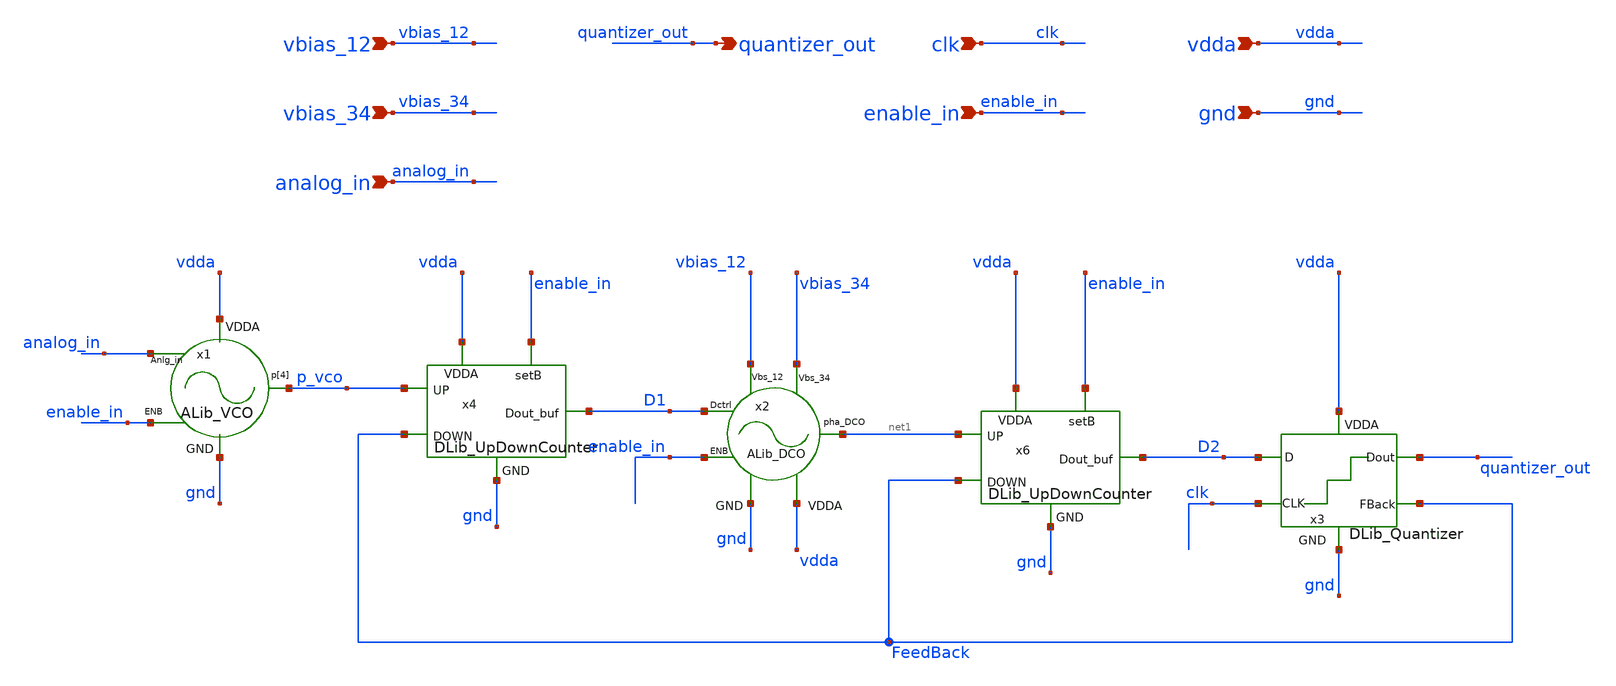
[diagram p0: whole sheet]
** sch_path: xschem/lib/vco_adc2.sch
**.subckt vco_adc2 vdda quantizer_out gnd enable_in clk vbias_34 analog_in vbias_12
*.ipin vdda
*.opin quantizer_out
*.ipin gnd
*.ipin enable_in
*.ipin clk
*.ipin vbias_34
*.ipin analog_in
*.ipin vbias_12
x1 analog_in enable_in p_vco vdda gnd ALib_VCO
x2 vbias_12 vbias_34 net1 D1 enable_in vdda gnd ALib_DCO
x3 vdda gnd clk quantizer_out FeedBack D2 DLib_Quantizer
x4 vdda gnd p_vco enable_in FeedBack D1 DLib_UpDownCounter
x6 vdda gnd net1 enable_in FeedBack D2 DLib_UpDownCounter
**.ends
.end
